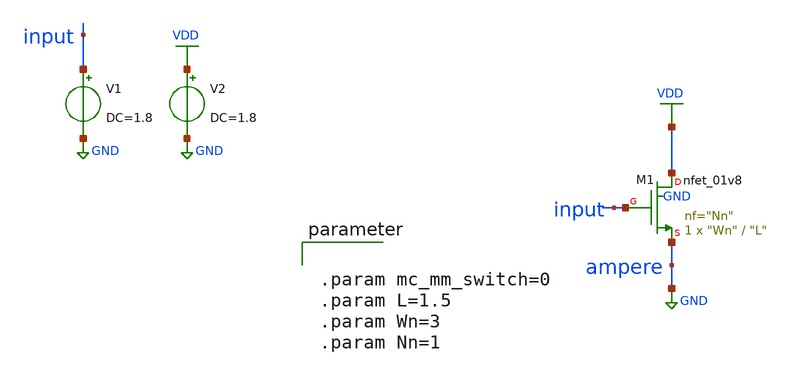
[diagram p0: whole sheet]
** sch_path: circuit_model/tb/NMOS.sch
**.subckt NMOS
XM1 VDD input GND GND sky130_fd_pr__nfet_01v8 L="L" W="Wn" nf="Nn" ad='int((nf+1)/2) * W/nf * 0.29' as='int((nf+2)/2) * W/nf * 0.29'
+ pd='2*int((nf+1)/2) * (W/nf + 0.29)' ps='2*int((nf+2)/2) * (W/nf + 0.29)' nrd='0.29 / W' nrs='0.29 / W'
+ sa=0 sb=0 sd=0 mult=1 m=1
V1 input GND DC=1.8
V2 VDD GND DC=1.8
**** begin user architecture code


.lib /home/dkits/efabless/mpw-5/pdks/sky130A/libs.tech/ngspice/sky130.lib.spice tt
.inc /home/dkits/efabless/mpw-5/pdks/sky130A/libs.ref/sky130_fd_sc_hd/spice/sky130_fd_sc_hd.spice




.param mc_mm_switch=0
.param L=1.5
.param Wn=3
.param Nn=1




.control
set nobreak
set numthread=11
TRAN 1n 6u
save i(M1, ampere)
plot input output
.endc


**** end user architecture code
**.ends
.GLOBAL VDD
.GLOBAL GND
.end
